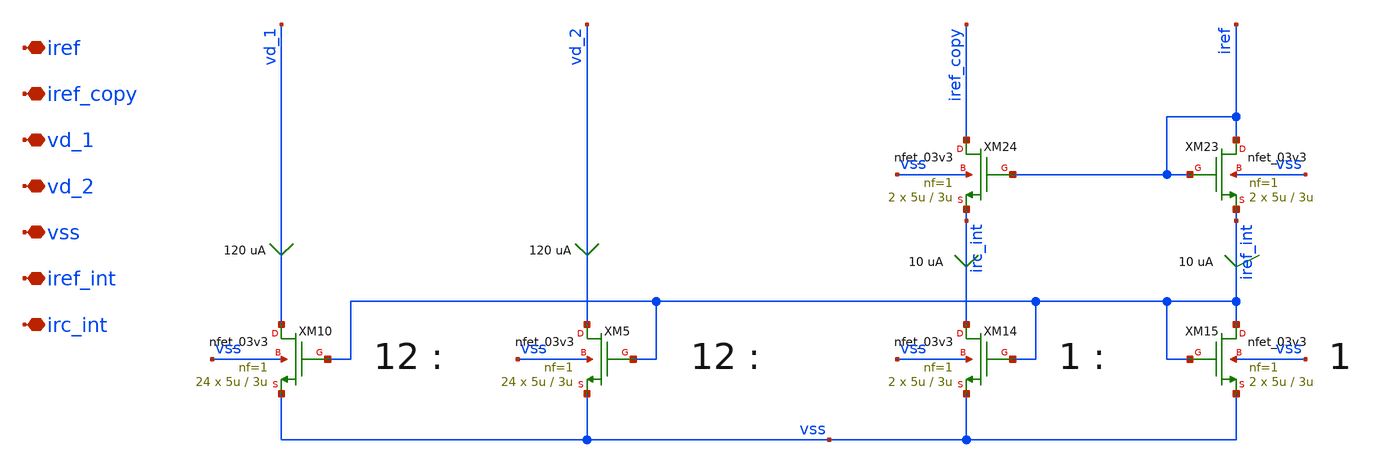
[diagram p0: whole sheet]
** sch_path: xschem/ccia_main_ota/b9_ccia_main_ota_s1_nmos_bias.sch
**.subckt b9_ccia_main_ota_s1_nmos_bias iref iref_copy vd_1 vd_2 vss iref_int irc_int
*.iopin iref
*.iopin iref_copy
*.iopin vd_1
*.iopin vd_2
*.iopin vss
*.iopin iref_int
*.iopin irc_int
XM14 irc_int iref_int vss vss nfet_03v3 L=3u W=5u nf=1 ad='int((nf+1)/2) * W/nf * 0.18u' as='int((nf+2)/2) * W/nf * 0.18u'
+ pd='2*int((nf+1)/2) * (W/nf + 0.18u)' ps='2*int((nf+2)/2) * (W/nf + 0.18u)' nrd='0.18u / W' nrs='0.18u / W'
+ sa=0 sb=0 sd=0 m=2
XM15 iref_int iref_int vss vss nfet_03v3 L=3u W=5u nf=1 ad='int((nf+1)/2) * W/nf * 0.18u' as='int((nf+2)/2) * W/nf * 0.18u'
+ pd='2*int((nf+1)/2) * (W/nf + 0.18u)' ps='2*int((nf+2)/2) * (W/nf + 0.18u)' nrd='0.18u / W' nrs='0.18u / W'
+ sa=0 sb=0 sd=0 m=2
XM10 vd_1 iref_int vss vss nfet_03v3 L=3u W=5u nf=1 ad='int((nf+1)/2) * W/nf * 0.18u' as='int((nf+2)/2) * W/nf * 0.18u'
+ pd='2*int((nf+1)/2) * (W/nf + 0.18u)' ps='2*int((nf+2)/2) * (W/nf + 0.18u)' nrd='0.18u / W' nrs='0.18u / W'
+ sa=0 sb=0 sd=0 m=24
XM5 vd_2 iref_int vss vss nfet_03v3 L=3u W=5u nf=1 ad='int((nf+1)/2) * W/nf * 0.18u' as='int((nf+2)/2) * W/nf * 0.18u'
+ pd='2*int((nf+1)/2) * (W/nf + 0.18u)' ps='2*int((nf+2)/2) * (W/nf + 0.18u)' nrd='0.18u / W' nrs='0.18u / W'
+ sa=0 sb=0 sd=0 m=24
XM23 iref iref iref_int vss nfet_03v3 L=3u W=5u nf=1 ad='int((nf+1)/2) * W/nf * 0.18u' as='int((nf+2)/2) * W/nf * 0.18u'
+ pd='2*int((nf+1)/2) * (W/nf + 0.18u)' ps='2*int((nf+2)/2) * (W/nf + 0.18u)' nrd='0.18u / W' nrs='0.18u / W'
+ sa=0 sb=0 sd=0 m=2
XM24 iref_copy iref irc_int vss nfet_03v3 L=3u W=5u nf=1 ad='int((nf+1)/2) * W/nf * 0.18u' as='int((nf+2)/2) * W/nf * 0.18u'
+ pd='2*int((nf+1)/2) * (W/nf + 0.18u)' ps='2*int((nf+2)/2) * (W/nf + 0.18u)' nrd='0.18u / W' nrs='0.18u / W'
+ sa=0 sb=0 sd=0 m=2
**.ends
.end
